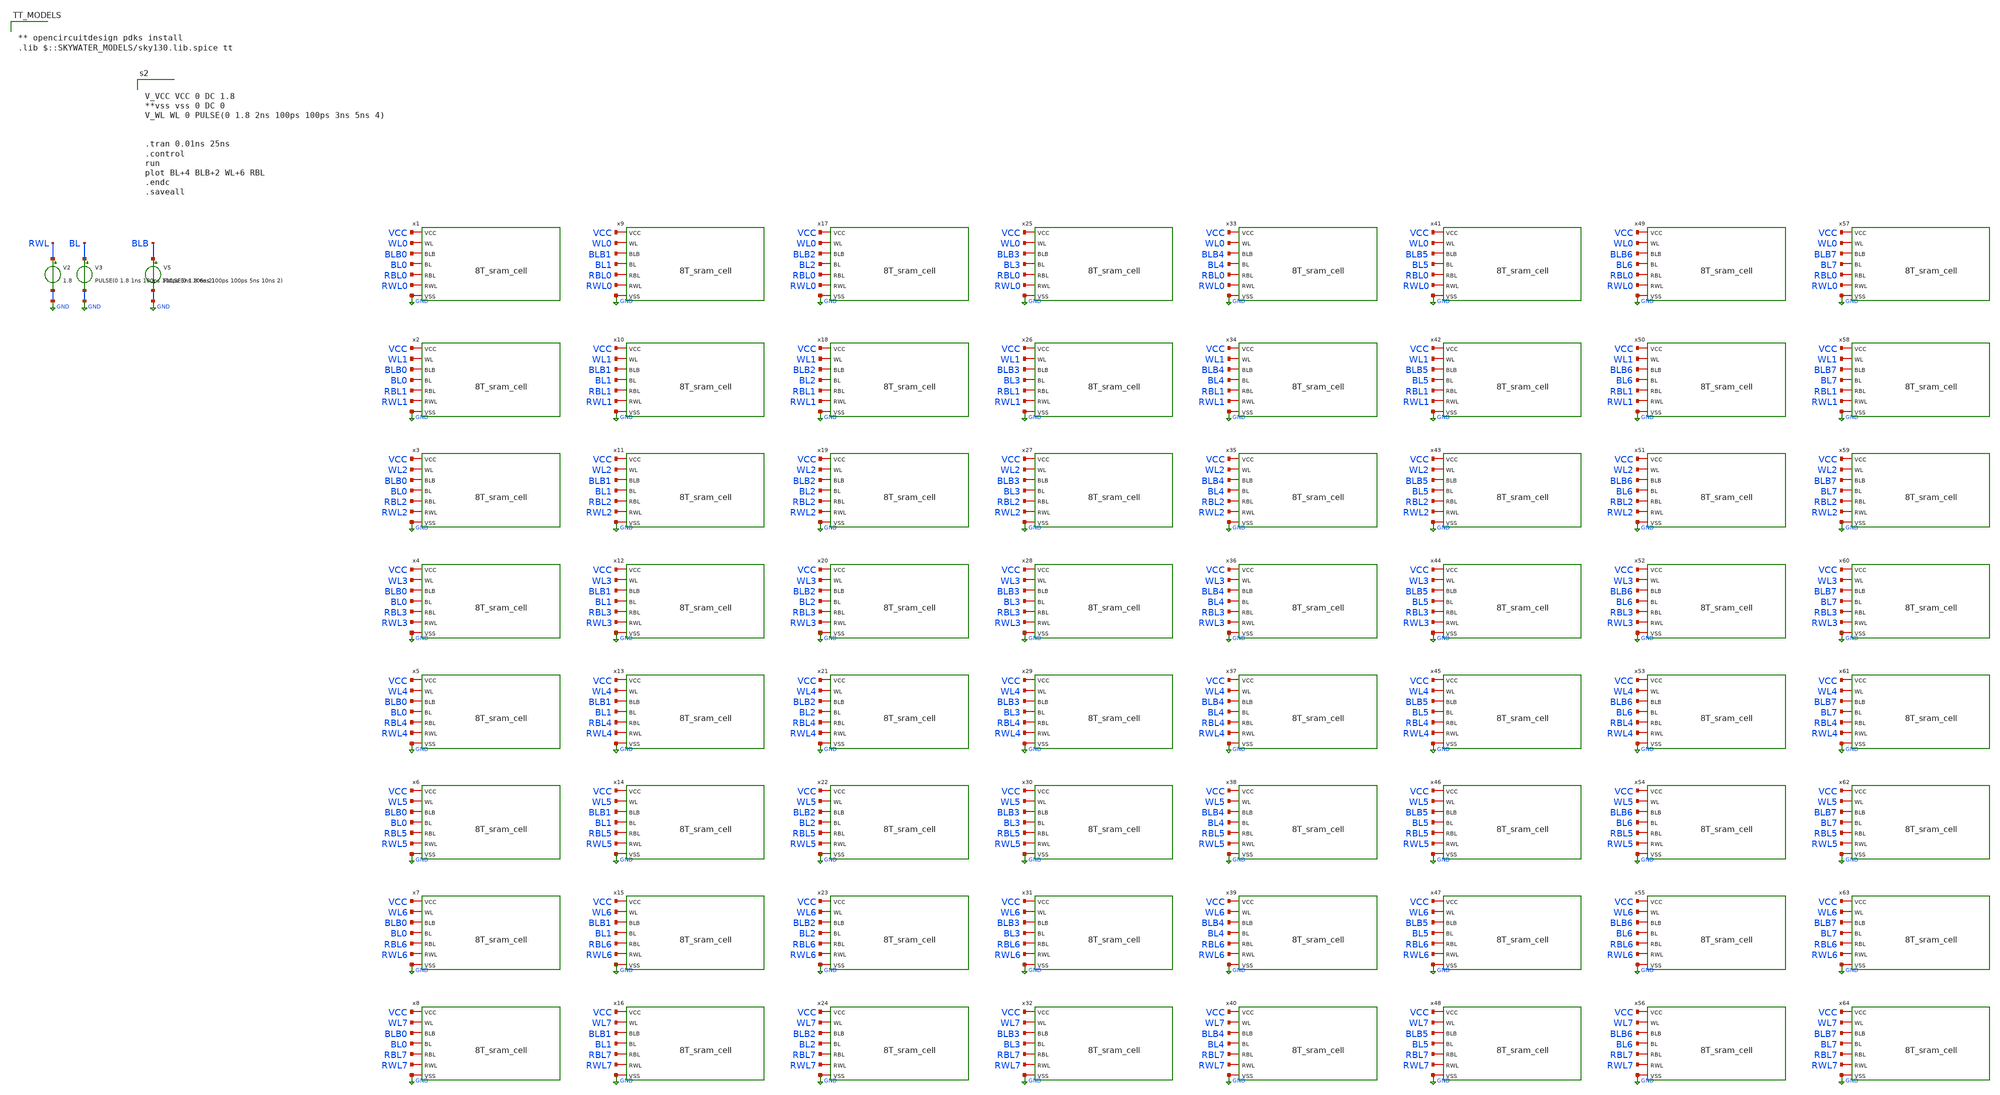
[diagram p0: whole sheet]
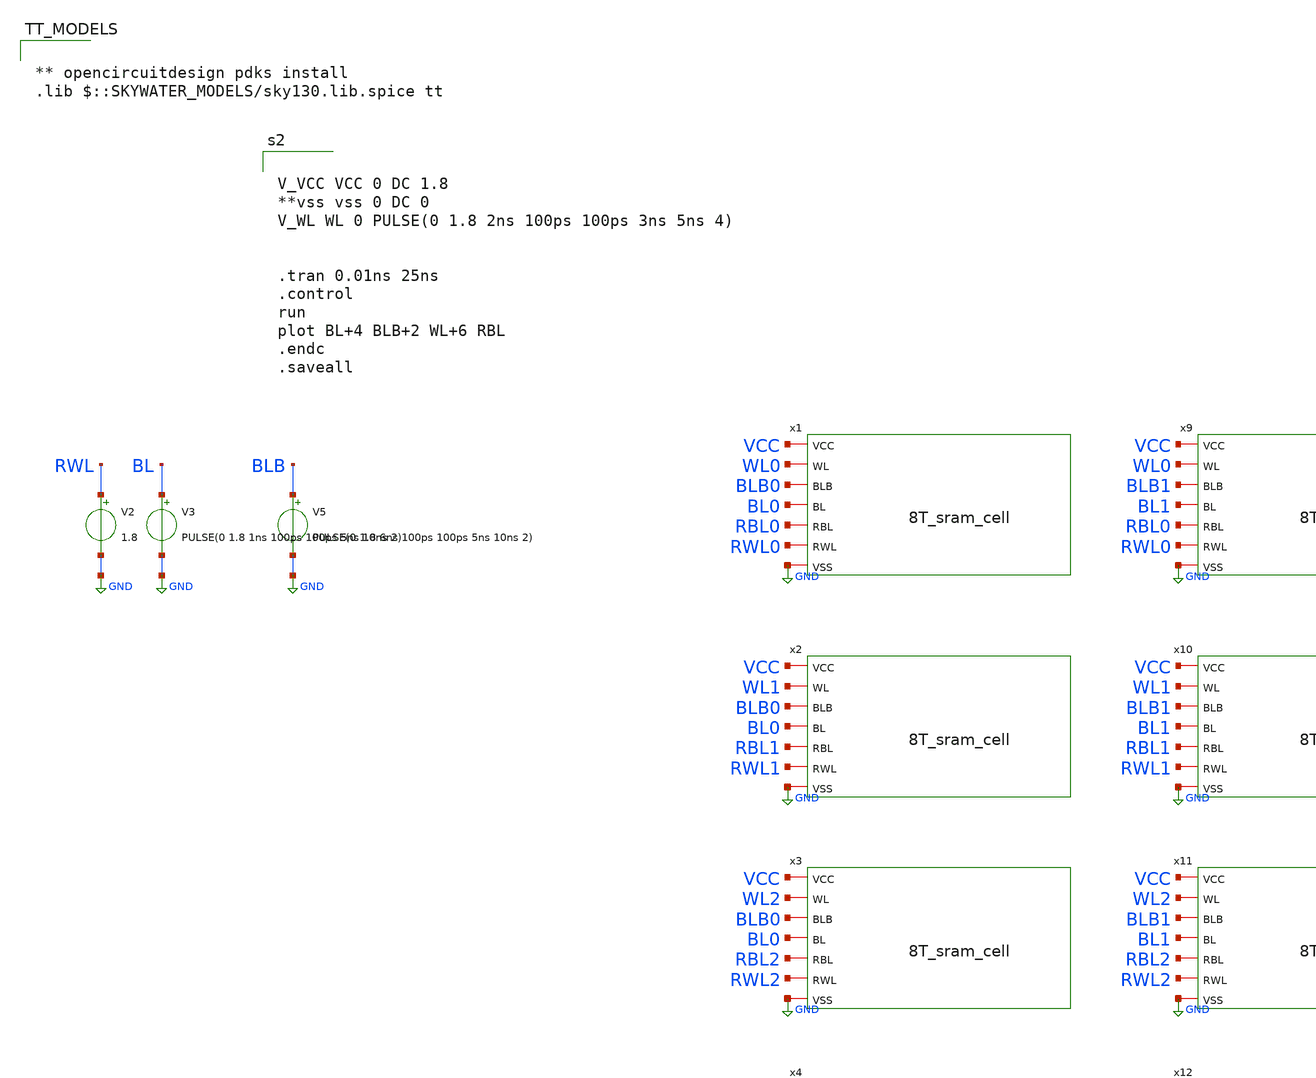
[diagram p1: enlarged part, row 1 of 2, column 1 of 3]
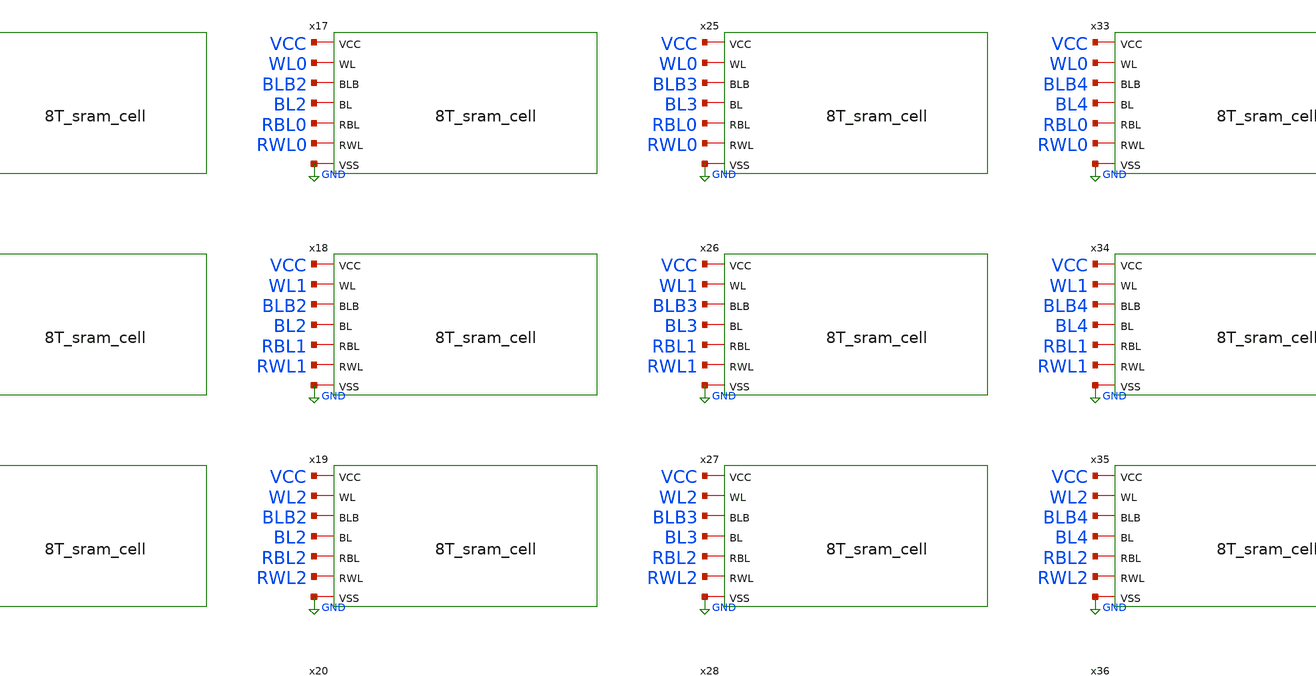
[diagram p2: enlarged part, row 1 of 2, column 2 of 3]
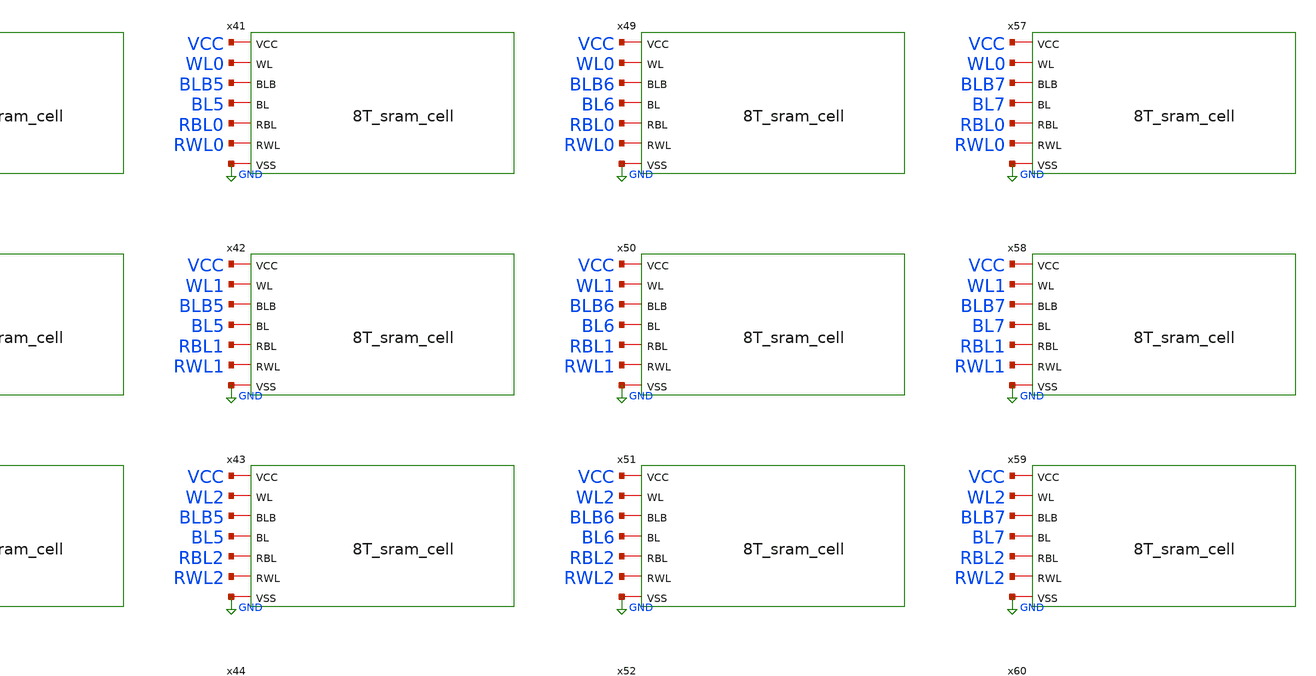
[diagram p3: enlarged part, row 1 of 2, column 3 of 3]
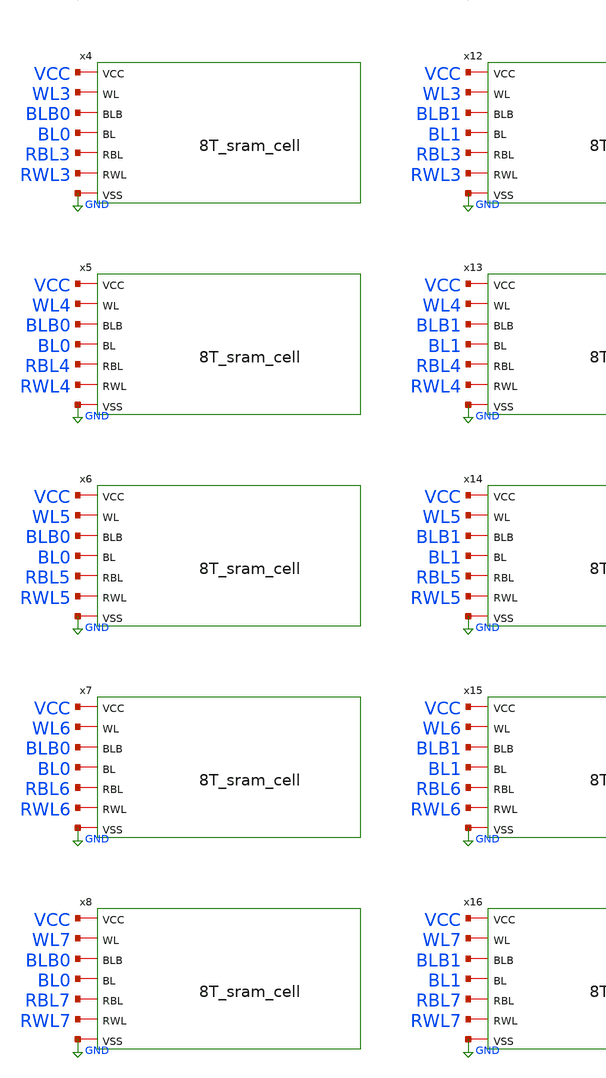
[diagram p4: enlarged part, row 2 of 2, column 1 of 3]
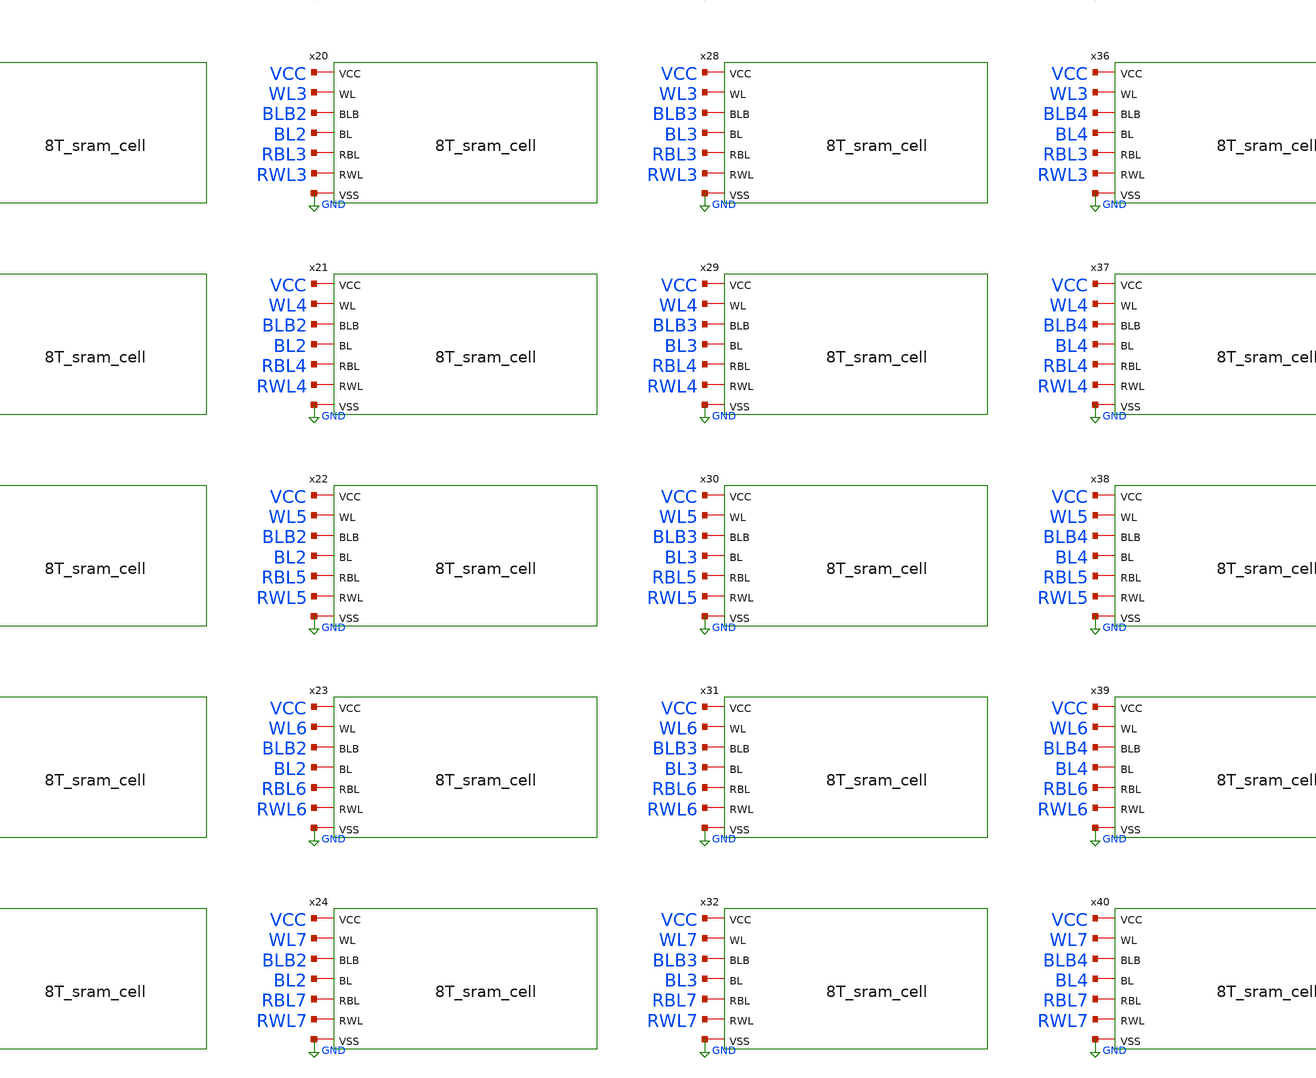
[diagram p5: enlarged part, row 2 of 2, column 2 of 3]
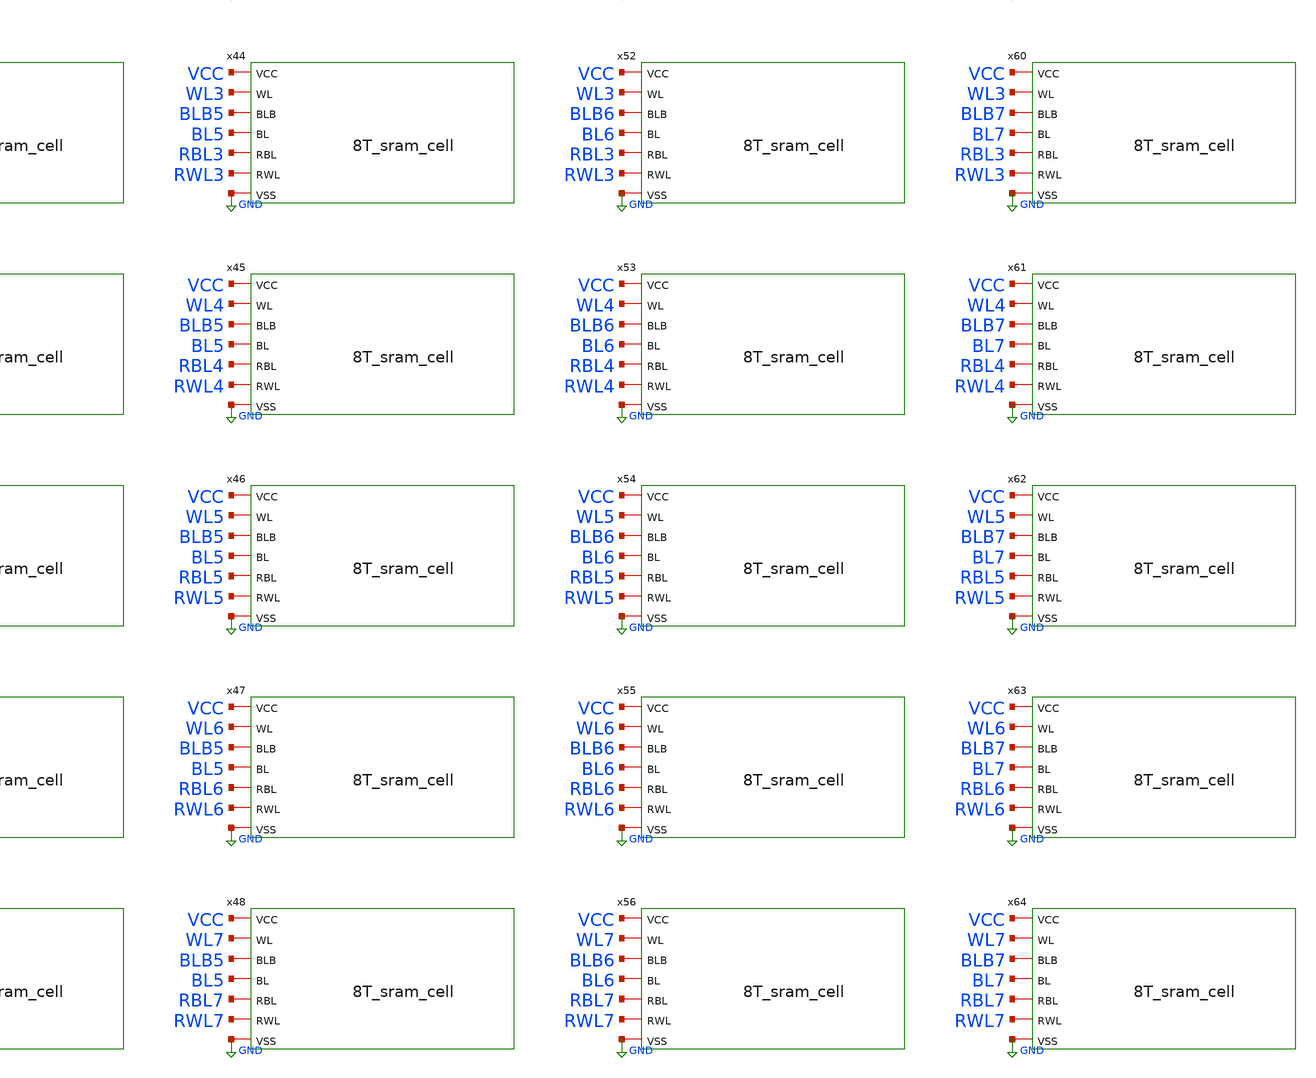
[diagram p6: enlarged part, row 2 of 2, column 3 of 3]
** sch_path: 8T_sram_array_test_py.sch
**.subckt 8T_sram_array_test_py
V2 RWL GND 1.8
V3 BL GND PULSE(0 1.8 1ns 100ps 100ps 5ns 10ns 2)
V5 BLB GND PULSE(0 1.8 6ns 100ps 100ps 5ns 10ns 2)
x1 VCC WL0 BLB0 BL0 RBL0 RWL0 GND 8T_sram_cell
x2 VCC WL1 BLB0 BL0 RBL1 RWL1 GND 8T_sram_cell
x3 VCC WL2 BLB0 BL0 RBL2 RWL2 GND 8T_sram_cell
x4 VCC WL3 BLB0 BL0 RBL3 RWL3 GND 8T_sram_cell
x5 VCC WL4 BLB0 BL0 RBL4 RWL4 GND 8T_sram_cell
x6 VCC WL5 BLB0 BL0 RBL5 RWL5 GND 8T_sram_cell
x7 VCC WL6 BLB0 BL0 RBL6 RWL6 GND 8T_sram_cell
x8 VCC WL7 BLB0 BL0 RBL7 RWL7 GND 8T_sram_cell
x9 VCC WL0 BLB1 BL1 RBL0 RWL0 GND 8T_sram_cell
x10 VCC WL1 BLB1 BL1 RBL1 RWL1 GND 8T_sram_cell
x11 VCC WL2 BLB1 BL1 RBL2 RWL2 GND 8T_sram_cell
x12 VCC WL3 BLB1 BL1 RBL3 RWL3 GND 8T_sram_cell
x13 VCC WL4 BLB1 BL1 RBL4 RWL4 GND 8T_sram_cell
x14 VCC WL5 BLB1 BL1 RBL5 RWL5 GND 8T_sram_cell
x15 VCC WL6 BLB1 BL1 RBL6 RWL6 GND 8T_sram_cell
x16 VCC WL7 BLB1 BL1 RBL7 RWL7 GND 8T_sram_cell
x17 VCC WL0 BLB2 BL2 RBL0 RWL0 GND 8T_sram_cell
x18 VCC WL1 BLB2 BL2 RBL1 RWL1 GND 8T_sram_cell
x19 VCC WL2 BLB2 BL2 RBL2 RWL2 GND 8T_sram_cell
x20 VCC WL3 BLB2 BL2 RBL3 RWL3 GND 8T_sram_cell
x21 VCC WL4 BLB2 BL2 RBL4 RWL4 GND 8T_sram_cell
x22 VCC WL5 BLB2 BL2 RBL5 RWL5 GND 8T_sram_cell
x23 VCC WL6 BLB2 BL2 RBL6 RWL6 GND 8T_sram_cell
x24 VCC WL7 BLB2 BL2 RBL7 RWL7 GND 8T_sram_cell
x25 VCC WL0 BLB3 BL3 RBL0 RWL0 GND 8T_sram_cell
x26 VCC WL1 BLB3 BL3 RBL1 RWL1 GND 8T_sram_cell
x27 VCC WL2 BLB3 BL3 RBL2 RWL2 GND 8T_sram_cell
x28 VCC WL3 BLB3 BL3 RBL3 RWL3 GND 8T_sram_cell
x29 VCC WL4 BLB3 BL3 RBL4 RWL4 GND 8T_sram_cell
x30 VCC WL5 BLB3 BL3 RBL5 RWL5 GND 8T_sram_cell
x31 VCC WL6 BLB3 BL3 RBL6 RWL6 GND 8T_sram_cell
x32 VCC WL7 BLB3 BL3 RBL7 RWL7 GND 8T_sram_cell
x33 VCC WL0 BLB4 BL4 RBL0 RWL0 GND 8T_sram_cell
x34 VCC WL1 BLB4 BL4 RBL1 RWL1 GND 8T_sram_cell
x35 VCC WL2 BLB4 BL4 RBL2 RWL2 GND 8T_sram_cell
x36 VCC WL3 BLB4 BL4 RBL3 RWL3 GND 8T_sram_cell
x37 VCC WL4 BLB4 BL4 RBL4 RWL4 GND 8T_sram_cell
x38 VCC WL5 BLB4 BL4 RBL5 RWL5 GND 8T_sram_cell
x39 VCC WL6 BLB4 BL4 RBL6 RWL6 GND 8T_sram_cell
x40 VCC WL7 BLB4 BL4 RBL7 RWL7 GND 8T_sram_cell
x41 VCC WL0 BLB5 BL5 RBL0 RWL0 GND 8T_sram_cell
x42 VCC WL1 BLB5 BL5 RBL1 RWL1 GND 8T_sram_cell
x43 VCC WL2 BLB5 BL5 RBL2 RWL2 GND 8T_sram_cell
x44 VCC WL3 BLB5 BL5 RBL3 RWL3 GND 8T_sram_cell
x45 VCC WL4 BLB5 BL5 RBL4 RWL4 GND 8T_sram_cell
x46 VCC WL5 BLB5 BL5 RBL5 RWL5 GND 8T_sram_cell
x47 VCC WL6 BLB5 BL5 RBL6 RWL6 GND 8T_sram_cell
x48 VCC WL7 BLB5 BL5 RBL7 RWL7 GND 8T_sram_cell
x49 VCC WL0 BLB6 BL6 RBL0 RWL0 GND 8T_sram_cell
x50 VCC WL1 BLB6 BL6 RBL1 RWL1 GND 8T_sram_cell
x51 VCC WL2 BLB6 BL6 RBL2 RWL2 GND 8T_sram_cell
x52 VCC WL3 BLB6 BL6 RBL3 RWL3 GND 8T_sram_cell
x53 VCC WL4 BLB6 BL6 RBL4 RWL4 GND 8T_sram_cell
x54 VCC WL5 BLB6 BL6 RBL5 RWL5 GND 8T_sram_cell
x55 VCC WL6 BLB6 BL6 RBL6 RWL6 GND 8T_sram_cell
x56 VCC WL7 BLB6 BL6 RBL7 RWL7 GND 8T_sram_cell
x57 VCC WL0 BLB7 BL7 RBL0 RWL0 GND 8T_sram_cell
x58 VCC WL1 BLB7 BL7 RBL1 RWL1 GND 8T_sram_cell
x59 VCC WL2 BLB7 BL7 RBL2 RWL2 GND 8T_sram_cell
x60 VCC WL3 BLB7 BL7 RBL3 RWL3 GND 8T_sram_cell
x61 VCC WL4 BLB7 BL7 RBL4 RWL4 GND 8T_sram_cell
x62 VCC WL5 BLB7 BL7 RBL5 RWL5 GND 8T_sram_cell
x63 VCC WL6 BLB7 BL7 RBL6 RWL6 GND 8T_sram_cell
x64 VCC WL7 BLB7 BL7 RBL7 RWL7 GND 8T_sram_cell
**** begin user architecture code


V_VCC VCC 0 DC 1.8
**vss vss 0 DC 0
V_WL WL 0 PULSE(0 1.8 2ns 100ps 100ps 3ns 5ns 4)


.tran 0.01ns 25ns
.control
run
plot BL+4 BLB+2 WL+6 RBL
.endc
.saveall




** opencircuitdesign pdks install
.lib $::SKYWATER_MODELS/sky130.lib.spice tt

**** end user architecture code
**.ends

* expanding   symbol:  8T_sram_cell.sym # of pins=7
** sym_path: 8T_sram_cell.sym
** sch_path: 8T_sram_cell.sch
.subckt 8T_sram_cell VCC WL BLB BL RBL RWL VSS
*.iopin VCC
*.iopin BLB
*.iopin WL
*.iopin BL
*.iopin VSS
*.iopin RBL
*.iopin RWL
XM1 q_bar q VSS VSS sky130_fd_pr__nfet_01v8 L=0.15 W=1 nf=1 ad='int((1 + 1)/2) * 1 / 1 * 0.29' as='int((1 + 2)/2) * 1 / 1 * 0.29'
+ pd='2*int((1 + 1)/2) * (1 / 1 + 0.29)' ps='2*int((1 + 2)/2) * (1 / 1 + 0.29)' nrd='0.29 / 1 ' nrs='0.29 / 1 '
+ sa=0 sb=0 sd=0 mult=1 m=1
XM2 q q_bar VSS VSS sky130_fd_pr__nfet_01v8 L=0.15 W=1 nf=1 ad='int((1 + 1)/2) * 1 / 1 * 0.29' as='int((1 + 2)/2) * 1 / 1 * 0.29'
+ pd='2*int((1 + 1)/2) * (1 / 1 + 0.29)' ps='2*int((1 + 2)/2) * (1 / 1 + 0.29)' nrd='0.29 / 1 ' nrs='0.29 / 1 '
+ sa=0 sb=0 sd=0 mult=1 m=1
XM3 q_bar q VCC VCC sky130_fd_pr__pfet_01v8 L=0.15 W=4 nf=1 ad='int((1 + 1)/2) * 4 / 1 * 0.29' as='int((1 + 2)/2) * 4 / 1 * 0.29'
+ pd='2*int((1 + 1)/2) * (4 / 1 + 0.29)' ps='2*int((1 + 2)/2) * (4 / 1 + 0.29)' nrd='0.29 / 4 ' nrs='0.29 / 4 '
+ sa=0 sb=0 sd=0 mult=1 m=1
XM4 q q_bar VCC VCC sky130_fd_pr__pfet_01v8 L=0.15 W=4 nf=1 ad='int((1 + 1)/2) * 4 / 1 * 0.29' as='int((1 + 2)/2) * 4 / 1 * 0.29'
+ pd='2*int((1 + 1)/2) * (4 / 1 + 0.29)' ps='2*int((1 + 2)/2) * (4 / 1 + 0.29)' nrd='0.29 / 4 ' nrs='0.29 / 4 '
+ sa=0 sb=0 sd=0 mult=1 m=1
XM5 BLB WL q_bar VSS sky130_fd_pr__nfet_01v8 L=0.15 W=1 nf=1 ad='int((1 + 1)/2) * 1 / 1 * 0.29' as='int((1 + 2)/2) * 1 / 1 * 0.29'
+ pd='2*int((1 + 1)/2) * (1 / 1 + 0.29)' ps='2*int((1 + 2)/2) * (1 / 1 + 0.29)' nrd='0.29 / 1 ' nrs='0.29 / 1 '
+ sa=0 sb=0 sd=0 mult=1 m=1
XM8 q WL BL VSS sky130_fd_pr__nfet_01v8 L=0.15 W=1 nf=1 ad='int((1 + 1)/2) * 1 / 1 * 0.29' as='int((1 + 2)/2) * 1 / 1 * 0.29'
+ pd='2*int((1 + 1)/2) * (1 / 1 + 0.29)' ps='2*int((1 + 2)/2) * (1 / 1 + 0.29)' nrd='0.29 / 1 ' nrs='0.29 / 1 '
+ sa=0 sb=0 sd=0 mult=1 m=1
XM6 net1 q_bar VSS VSS sky130_fd_pr__nfet_01v8 L=0.15 W=1 nf=1 ad='int((1 + 1)/2) * 1 / 1 * 0.29' as='int((1 + 2)/2) * 1 / 1 * 0.29'
+ pd='2*int((1 + 1)/2) * (1 / 1 + 0.29)' ps='2*int((1 + 2)/2) * (1 / 1 + 0.29)' nrd='0.29 / 1 ' nrs='0.29 / 1 '
+ sa=0 sb=0 sd=0 mult=1 m=1
XM7 RBL RWL net1 VSS sky130_fd_pr__nfet_01v8 L=0.15 W=1 nf=1 ad='int((1 + 1)/2) * 1 / 1 * 0.29' as='int((1 + 2)/2) * 1 / 1 * 0.29'
+ pd='2*int((1 + 1)/2) * (1 / 1 + 0.29)' ps='2*int((1 + 2)/2) * (1 / 1 + 0.29)' nrd='0.29 / 1 ' nrs='0.29 / 1 '
+ sa=0 sb=0 sd=0 mult=1 m=1
.ends

.GLOBAL GND
.end
